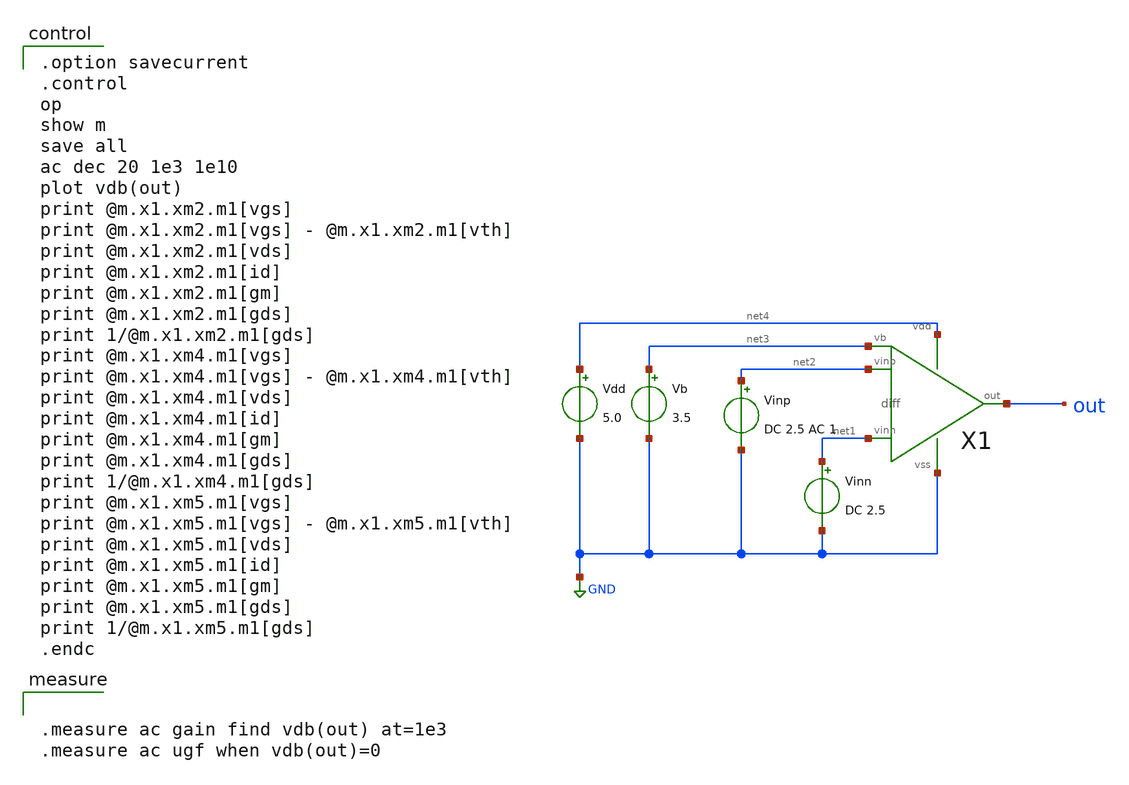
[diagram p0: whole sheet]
** sch_path: member_project/opamp/houta/diff_ac.sch
**.subckt diff_ac
Vdd net4 GND 5.0
Vb net3 GND 3.5
Vinn net1 GND DC 2.5
Vinp net2 GND DC 2.5 AC 1
X1 net2 net1 out net4 GND net3 diff
**** begin user architecture code

.option savecurrent
.control
op
show m
save all
ac dec 20 1e3 1e10
plot vdb(out)
print @m.x1.xm2.m1[vgs]
print @m.x1.xm2.m1[vgs] - @m.x1.xm2.m1[vth]
print @m.x1.xm2.m1[vds]
print @m.x1.xm2.m1[id]
print @m.x1.xm2.m1[gm]
print @m.x1.xm2.m1[gds]
print 1/@m.x1.xm2.m1[gds]
print @m.x1.xm4.m1[vgs]
print @m.x1.xm4.m1[vgs] - @m.x1.xm4.m1[vth]
print @m.x1.xm4.m1[vds]
print @m.x1.xm4.m1[id]
print @m.x1.xm4.m1[gm]
print @m.x1.xm4.m1[gds]
print 1/@m.x1.xm4.m1[gds]
print @m.x1.xm5.m1[vgs]
print @m.x1.xm5.m1[vgs] - @m.x1.xm5.m1[vth]
print @m.x1.xm5.m1[vds]
print @m.x1.xm5.m1[id]
print @m.x1.xm5.m1[gm]
print @m.x1.xm5.m1[gds]
print 1/@m.x1.xm5.m1[gds]
.endc



.measure ac gain find vdb(out) at=1e3
.measure ac ugf when vdb(out)=0


 .include $::LIB/ip62_models
**** end user architecture code
**.ends

* expanding   symbol:  diff.sym # of pins=6
** sym_path: diff.sym
** sch_path: diff.sch
.subckt diff vinp vinn out vdd vss vb
*.ipin vinn
*.ipin vinp
*.ipin vb
*.opin out
*.iopin vdd
*.iopin vss
XM5 net2 vb vdd vdd PMOS w=220u l=2u as=0 ad=0 ps=0 pd=0 nrd=0 nrs=0 m=1
XM1 net1 vinn net2 net2 PMOS w=500u l=2u as=0 ad=0 ps=0 pd=0 nrd=0 nrs=0 m=1
XM2 out vinp net2 net2 PMOS w=500u l=2u as=0 ad=0 ps=0 pd=0 nrd=0 nrs=0 m=1
XM3 net1 net1 vss vss NMOS w=40u l=2u as=0 ad=0 ps=0 pd=0 nrd=0 nrs=0 m=1
XM4 out net1 vss vss NMOS w=40u l=2u as=0 ad=0 ps=0 pd=0 nrd=0 nrs=0 m=1
.ends

.GLOBAL GND
.end
